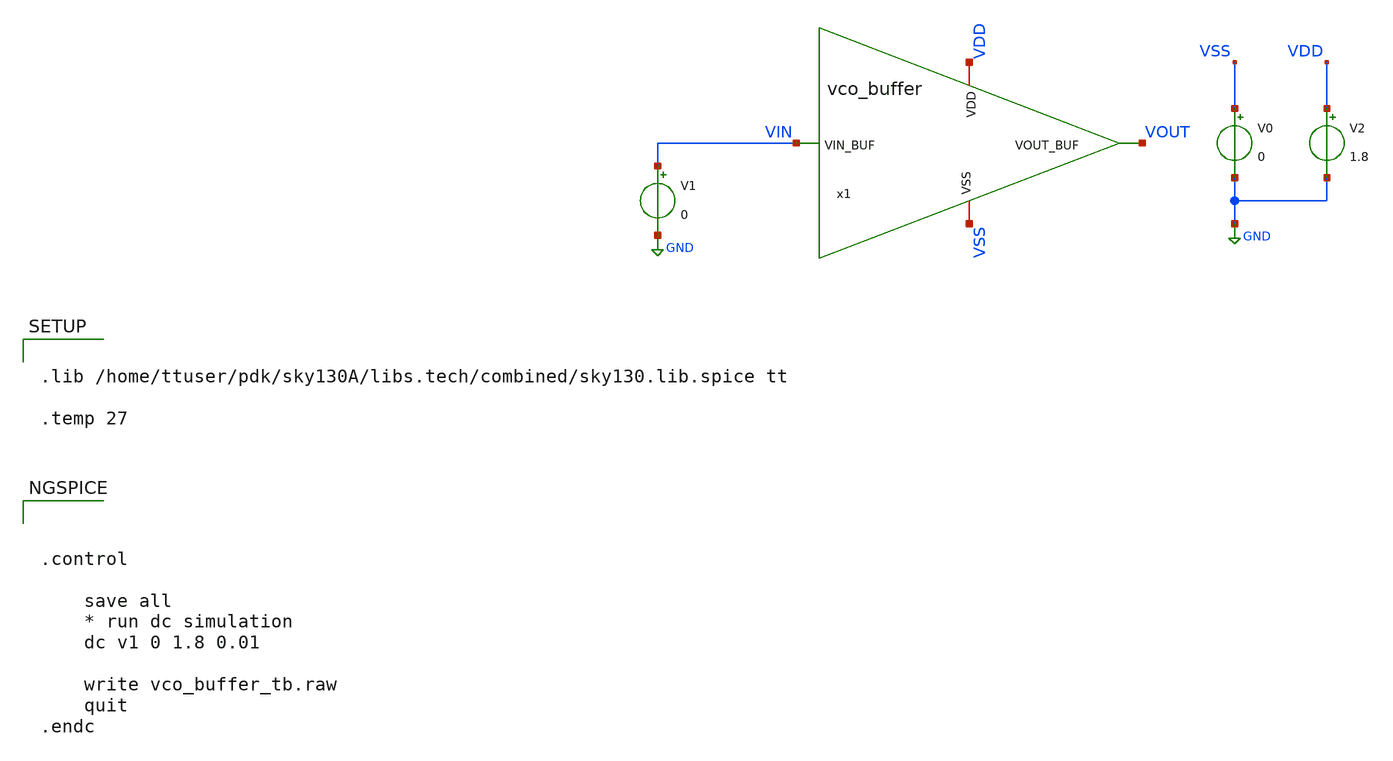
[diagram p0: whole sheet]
** sch_path: xschem/vco_buffer_tb.sch
**.subckt vco_buffer_tb
V0 VSS GND 0
V2 VDD GND 1.8
x1 VDD VSS VIN VOUT vco_buffer
V1 VIN GND 0
**** begin user architecture code



.control

    save all
    * run dc simulation
    dc v1 0 1.8 0.01

    write vco_buffer_tb.raw
    quit
.endc




.lib /home/ttuser/pdk/sky130A/libs.tech/combined/sky130.lib.spice tt

.temp 27


**** end user architecture code
**.ends

* expanding   symbol:  vco_buffer.sym # of pins=4
** sym_path: xschem/vco_buffer.sym
** sch_path: xschem/vco_buffer.sch
.subckt vco_buffer VDD VSS VIN_BUF VOUT_BUF
*.iopin VDD
*.iopin VSS
*.ipin VIN_BUF
*.opin VOUT_BUF
x1 VDD VIN_BUF INT_BUF VSS vco_inverter
x2 VDD INT_BUF VOUT_BUF VSS vco_inverter
.ends


* expanding   symbol:  vco_inverter.sym # of pins=4
** sym_path: xschem/vco_inverter.sym
** sch_path: xschem/vco_inverter.sch
.subckt vco_inverter VDD VIN_INV VOUT_INV VSS
*.iopin VDD
*.iopin VSS
*.ipin VIN_INV
*.opin VOUT_INV
XM1 VOUT_INV VIN_INV VSS VSS sky130_fd_pr__nfet_01v8 L=0.15 W=1 nf=1 ad='int((nf+1)/2) * W/nf * 0.29'
+ as='int((nf+2)/2) * W/nf * 0.29' pd='2*int((nf+1)/2) * (W/nf + 0.29)' ps='2*int((nf+2)/2) * (W/nf + 0.29)'
+ nrd='0.29 / W' nrs='0.29 / W' sa=0 sb=0 sd=0 mult=1 m=1
XM2 VOUT_INV VIN_INV VDD VDD sky130_fd_pr__pfet_01v8 L=0.15 W=1 nf=1 ad='int((nf+1)/2) * W/nf * 0.29'
+ as='int((nf+2)/2) * W/nf * 0.29' pd='2*int((nf+1)/2) * (W/nf + 0.29)' ps='2*int((nf+2)/2) * (W/nf + 0.29)'
+ nrd='0.29 / W' nrs='0.29 / W' sa=0 sb=0 sd=0 mult=1 m=1
.ends

.GLOBAL GND
.end
